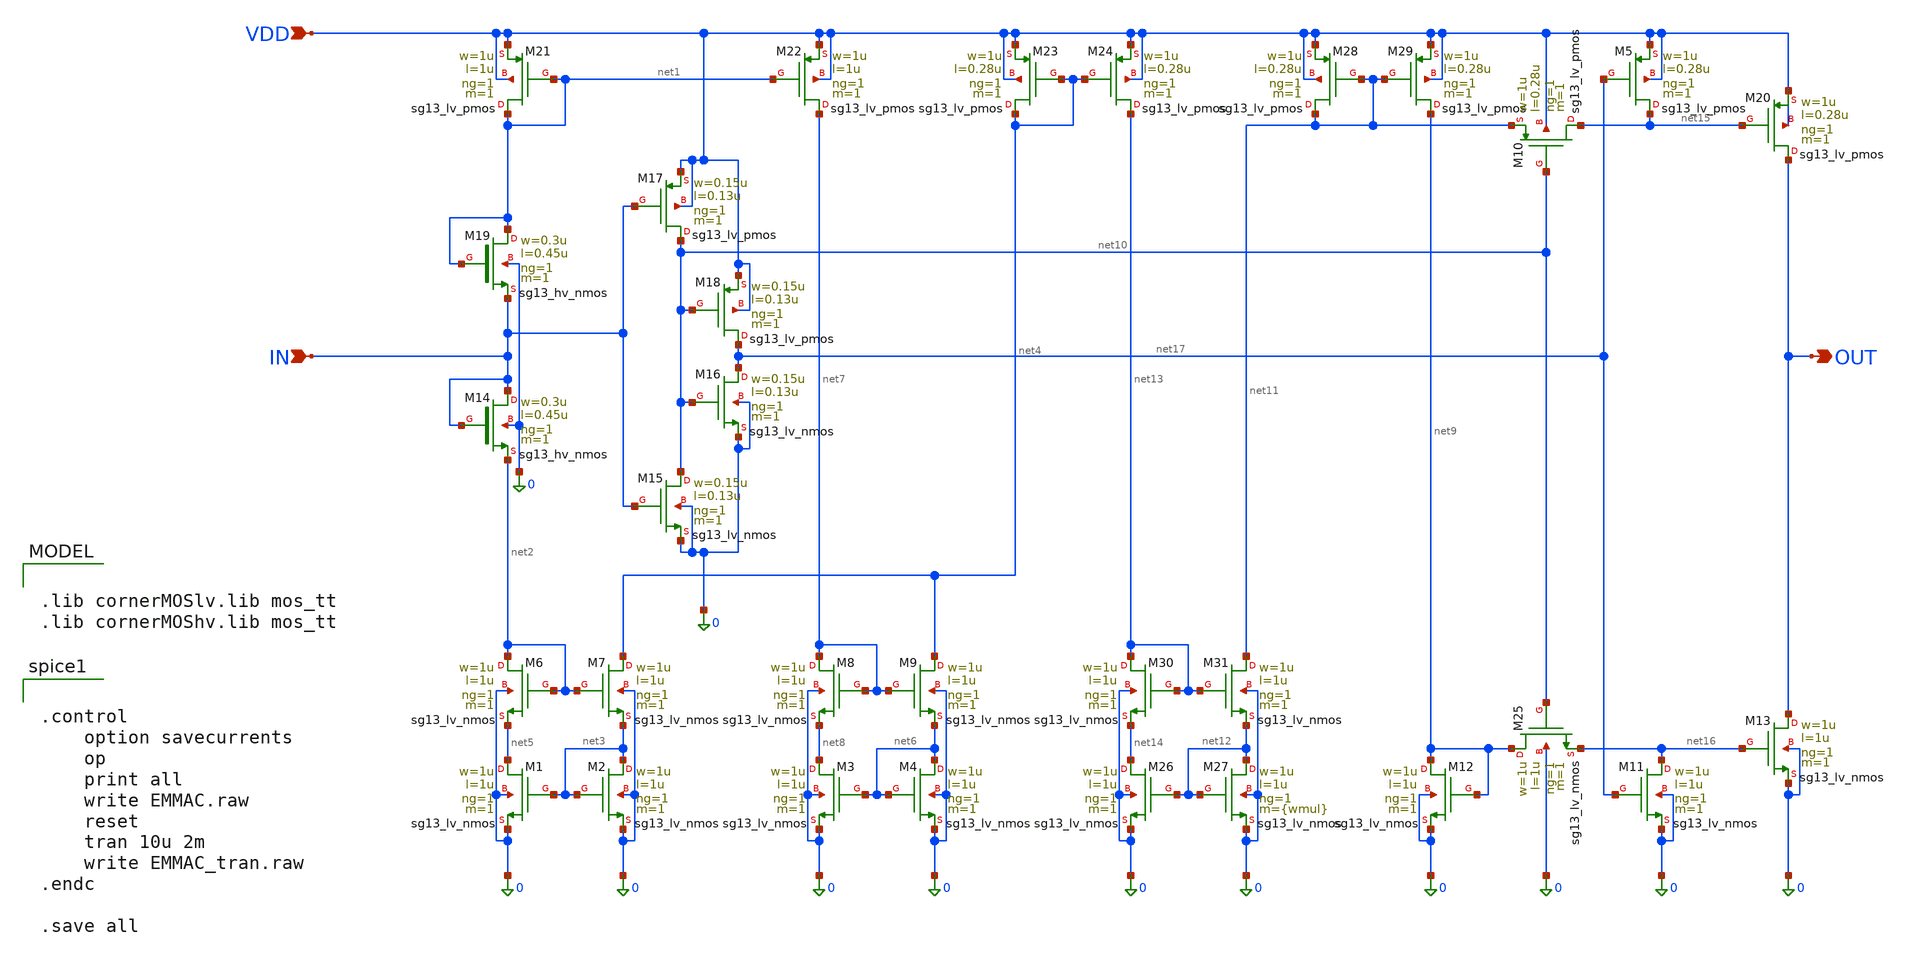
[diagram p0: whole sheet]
** sch_path: src/analog_mac/EMMAC_Block_v3.sch
**.subckt EMMAC_Block_v3 OUT IN VDD
*.opin OUT
*.ipin IN
*.ipin VDD
XM1 net5 net3 0 0 sg13_lv_nmos w=1u l=1u ng=1 m=1 mm_ok=1
XM2 net3 net3 0 0 sg13_lv_nmos w=1u l=1u ng=1 m=1 mm_ok=1
XM21 net1 net1 VDD VDD sg13_lv_pmos w=1u l=1u ng=1 m=1 mm_ok=1
XM22 net7 net1 VDD VDD sg13_lv_pmos w=1u l=1u ng=1 m=1 mm_ok=1
XM6 net2 net2 net5 0 sg13_lv_nmos w=1u l=1u ng=1 m=1 mm_ok=1
XM7 net4 net2 net3 0 sg13_lv_nmos w=1u l=1u ng=1 m=1 mm_ok=1
XM3 net8 net6 0 0 sg13_lv_nmos w=1u l=1u ng=1 m=1 mm_ok=1
XM4 net6 net6 0 0 sg13_lv_nmos w=1u l=1u ng=1 m=1 mm_ok=1
XM8 net7 net7 net8 0 sg13_lv_nmos w=1u l=1u ng=1 m=1 mm_ok=1
XM9 net4 net7 net6 0 sg13_lv_nmos w=1u l=1u ng=1 m=1 mm_ok=1
XM23 net4 net4 VDD VDD sg13_lv_pmos w=1u l=0.28u ng=1 m=1 mm_ok=1
XM24 net13 net4 VDD VDD sg13_lv_pmos w=1u l=0.28u ng=1 m=1 mm_ok=1
XM19 net1 net1 IN 0 sg13_hv_nmos w=0.3u l=0.45u ng=1 m=1 mm_ok=1
XM14 IN IN net2 0 sg13_hv_nmos w=0.3u l=0.45u ng=1 m=1 mm_ok=1
XM20 OUT net15 VDD VDD sg13_lv_pmos w=1u l=0.28u ng=1 m=1 mm_ok=1
XM12 net9 net9 0 0 sg13_lv_nmos w=1u l=1u ng=1 m=1 mm_ok=1
XM13 OUT net16 0 0 sg13_lv_nmos w=1u l=1u ng=1 m=1 mm_ok=1
XM15 net10 IN 0 0 sg13_lv_nmos w=0.15u l=0.13u ng=1 m=1 mm_ok=1
XM17 net10 IN VDD VDD sg13_lv_pmos w=0.15u l=0.13u ng=1 m=1 mm_ok=1
XM16 net17 net10 0 0 sg13_lv_nmos w=0.15u l=0.13u ng=1 m=1 mm_ok=1
XM18 net17 net10 VDD VDD sg13_lv_pmos w=0.15u l=0.13u ng=1 m=1 mm_ok=1
XM28 net11 net11 VDD VDD sg13_lv_pmos w=1u l=0.28u ng=1 m=1 mm_ok=1
XM29 net9 net11 VDD VDD sg13_lv_pmos w=1u l=0.28u ng=1 m=1 mm_ok=1
XM26 net14 net12 0 0 sg13_lv_nmos w=1u l=1u ng=1 m=1 mm_ok=1
XM27 net12 net12 0 0 sg13_lv_nmos w=1u l=1u ng=1 m={wmul} mm_ok=1
XM30 net13 net13 net14 0 sg13_lv_nmos w=1u l=1u ng=1 m=1 mm_ok=1
XM31 net11 net13 net12 0 sg13_lv_nmos w=1u l=1u ng=1 m=1 mm_ok=1
XM5 net15 net17 VDD VDD sg13_lv_pmos w=1u l=0.28u ng=1 m=1 mm_ok=1
XM10 net15 net10 net11 VDD sg13_lv_pmos w=1u l=0.28u ng=1 m=1 mm_ok=1
XM11 net16 net17 0 0 sg13_lv_nmos w=1u l=1u ng=1 m=1 mm_ok=1
XM25 net9 net10 net16 0 sg13_lv_nmos w=1u l=1u ng=1 m=1 mm_ok=1
**** begin user architecture code

.lib cornerMOSlv.lib mos_tt
.lib cornerMOShv.lib mos_tt



.control
	option savecurrents
	op
	print all
	write EMMAC.raw
	reset
	tran 10u 2m
	write EMMAC_tran.raw
.endc

.save all


**** end user architecture code
**.ends
.end
